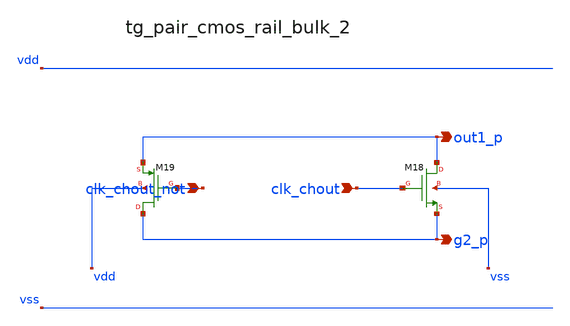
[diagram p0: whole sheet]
** sch_path: analog-db/raw/ia_003_fan_chopper_pf/hier/blocks/tg_pair_cmos_rail_bulk_2.sch
**.subckt tg_pair_cmos_rail_bulk_2 clk_chout_not clk_chout out1_p g2_p
*.ipin clk_chout_not
*.ipin clk_chout
*.opin out1_p
*.opin g2_p
XM18 out1_p clk_chout g2_p vss sg13_lv_nmos w=x_dut_xm18_w l=x_dut_xm18_l ng=1 m=x_dut_xm18_m
XM19 g2_p clk_chout_not out1_p vdd sg13_lv_pmos w=x_dut_xm19_w l=x_dut_xm19_l ng=1 m=x_dut_xm19_m
**.ends
.end
